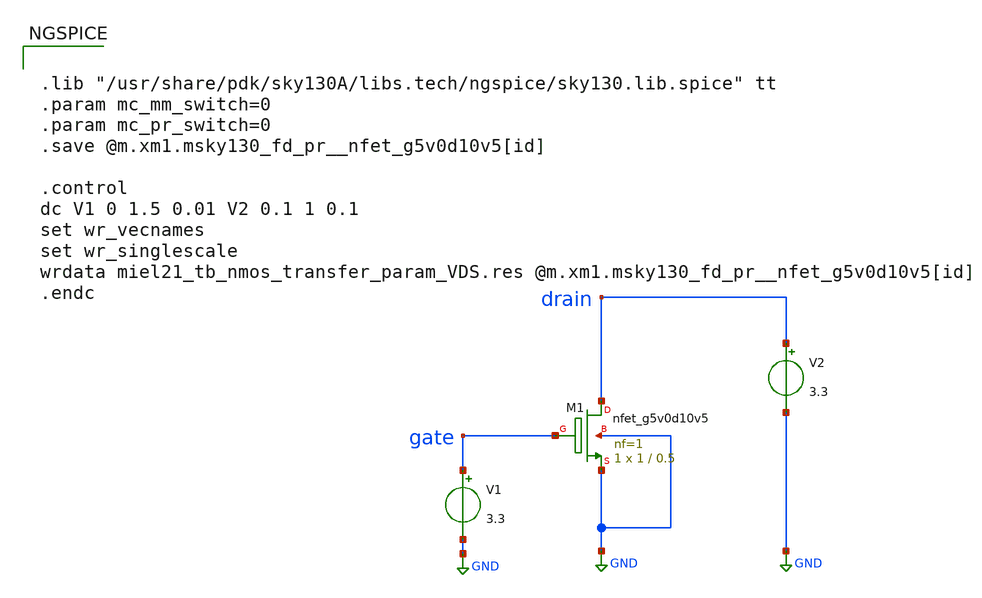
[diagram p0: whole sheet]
** sch_path: dev/opamp/miel21_tb_nmos_transfer_param_VDS.sch
**.subckt miel21_tb_nmos_transfer_param_VDS
V1 gate GND 3.3
V2 drain GND 3.3
XM1 drain gate GND GND sky130_fd_pr__nfet_g5v0d10v5 L=0.5 W=1 nf=1 ad='int((nf+1)/2) * W/nf * 0.29' as='int((nf+2)/2) * W/nf * 0.29'
+ pd='2*int((nf+1)/2) * (W/nf + 0.29)' ps='2*int((nf+2)/2) * (W/nf + 0.29)' nrd='0.29 / W' nrs='0.29 / W'
+ sa=0 sb=0 sd=0 mult=1 m=1
**** begin user architecture code


.lib "/usr/share/pdk/sky130A/libs.tech/ngspice/sky130.lib.spice" tt
.param mc_mm_switch=0
.param mc_pr_switch=0
.save @m.xm1.msky130_fd_pr__nfet_g5v0d10v5[id]

.control
dc V1 0 1.5 0.01 V2 0.1 1 0.1
set wr_vecnames
set wr_singlescale
wrdata miel21_tb_nmos_transfer_param_VDS.res @m.xm1.msky130_fd_pr__nfet_g5v0d10v5[id]
.endc


**** end user architecture code
**.ends
.GLOBAL GND
.end
